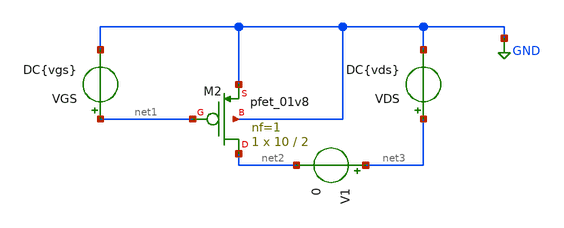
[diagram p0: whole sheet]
** sch_path: tp1_2.sch
**.subckt tp1_2
VGS net1 GND DC{vgs}
VDS net3 GND DC{vds}
XM2 net2 net1 GND GND sky130_fd_pr__pfet_01v8 L=2 W=10 nf=1 ad='int((nf+1)/2) * W/nf * 0.29' as='int((nf+2)/2) * W/nf * 0.29'
+ pd='2*int((nf+1)/2) * (W/nf + 0.29)' ps='2*int((nf+2)/2) * (W/nf + 0.29)' nrd='0.29 / W' nrs='0.29 / W'
+ sa=0 sb=0 sd=0 mult=1 m=1
V1 net3 net2 0
**** begin user architecture code



* Parameters
.param vds = -1.8
.param vgs = -0.9
.options TEMPS = 27.0

* Models
.lib ~/skywater/skywater-pdk/libraries/sky130_fd_pr_ngspice/latest/models/corners/sky130.lib TT

* Data to save
.save all  @M.XM2.msky130_fd_pr__pfet_01v8[id]  @M.XM2.msky130_fd_pr__pfet_01v8[gm]  @M.XM2.msky130_fd_pr__pfet_01v8[vth]  @M.XM2.msky130_fd_pr__pfet_01v8[vds]  @M.XM2.msky130_fd_pr__pfet_01v8[vdsat]  @M.XM2.msky130_fd_pr__pfet_01v8[vgs]  I(V1);


* Simulation
.control
  dc VDS 0 -1.8 -0.01 VGS 0 -1.8 -0.3
  setplot dc1
  plot I(V1) ylabel Id xlabel Vds title 'Id vs Vds vs Vgs'
  set filetype = ascii
  write tp1_2_dc1.raw

  reset
  dc VGS 0 -1.8 -0.01
  setplot dc2
  plot I(V1) ylabel Id xlabel Vgs title 'Id vs Vgs'
  set filetype = ascii
  write tp1_2_dc2.raw


  reset
  unset filetype
  op
  save all
  write tp1_2.raw


.endc



.end


**** end user architecture code
**.ends
.GLOBAL GND
.end
